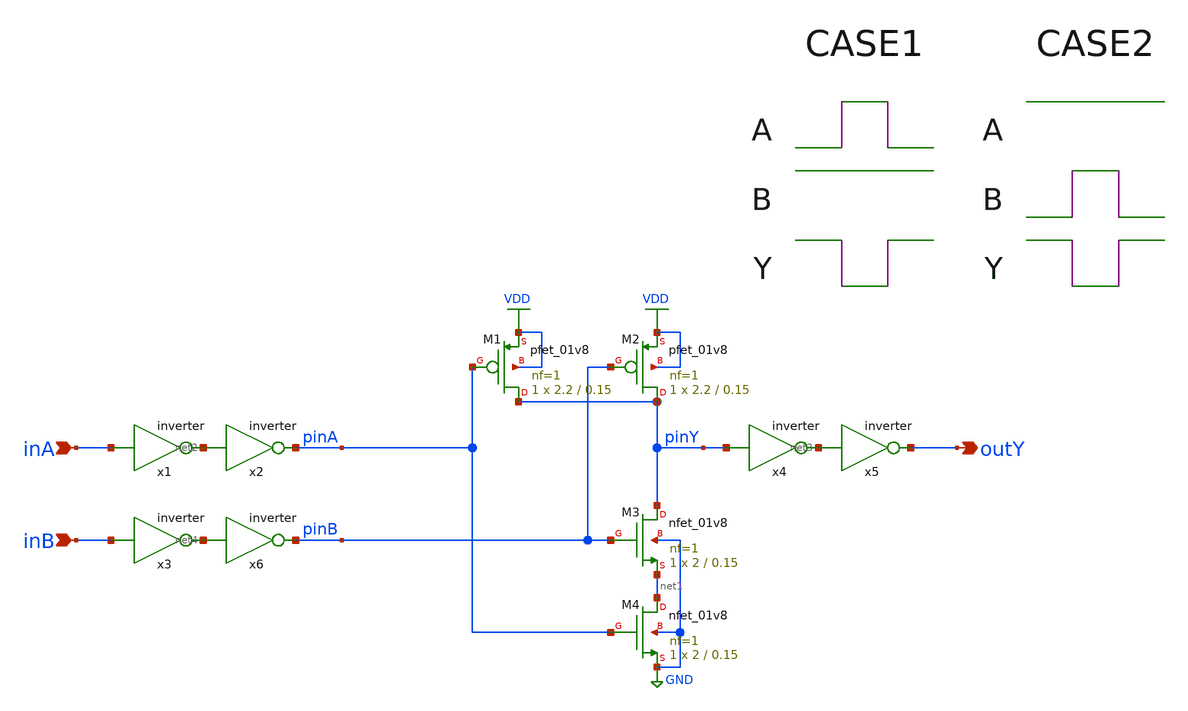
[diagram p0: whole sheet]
** sch_path: nand_delay.sch
**.subckt nand_delay inA outY inB
*.ipin inA
*.opin outY
*.ipin inB
x1 net2 inA inverter
x2 pinA net2 inverter
x4 net3 pinY inverter
x5 outY net3 inverter
x3 net4 inB inverter
x6 pinB net4 inverter
XM1 pinY pinA VDD VDD sky130_fd_pr__pfet_01v8 L=0.15 W=2.2 nf=1 ad='int((nf+1)/2) * W/nf * 0.29' as='int((nf+2)/2) * W/nf * 0.29'
+ pd='2*int((nf+1)/2) * (W/nf + 0.29)' ps='2*int((nf+2)/2) * (W/nf + 0.29)' nrd='0.29 / W' nrs='0.29 / W'
+ sa=0 sb=0 sd=0 mult=1 m=1
XM2 pinY pinB VDD VDD sky130_fd_pr__pfet_01v8 L=0.15 W=2.2 nf=1 ad='int((nf+1)/2) * W/nf * 0.29' as='int((nf+2)/2) * W/nf * 0.29'
+ pd='2*int((nf+1)/2) * (W/nf + 0.29)' ps='2*int((nf+2)/2) * (W/nf + 0.29)' nrd='0.29 / W' nrs='0.29 / W'
+ sa=0 sb=0 sd=0 mult=1 m=1
XM3 pinY pinB net1 GND sky130_fd_pr__nfet_01v8 L=0.15 W=2 nf=1 ad='int((nf+1)/2) * W/nf * 0.29' as='int((nf+2)/2) * W/nf * 0.29'
+ pd='2*int((nf+1)/2) * (W/nf + 0.29)' ps='2*int((nf+2)/2) * (W/nf + 0.29)' nrd='0.29 / W' nrs='0.29 / W'
+ sa=0 sb=0 sd=0 mult=1 m=1
XM4 net1 pinA GND GND sky130_fd_pr__nfet_01v8 L=0.15 W=2 nf=1 ad='int((nf+1)/2) * W/nf * 0.29' as='int((nf+2)/2) * W/nf * 0.29'
+ pd='2*int((nf+1)/2) * (W/nf + 0.29)' ps='2*int((nf+2)/2) * (W/nf + 0.29)' nrd='0.29 / W' nrs='0.29 / W'
+ sa=0 sb=0 sd=0 mult=1 m=1
**** begin user architecture code


VA inA 0 dc 0
VB inB 0 dc 0
VD VDD 0 dc 1.8
.control
alter @va[PULSE] [ 0 1.8 1n 40p 40p 1n 3n ]
alter @vb[PULSE] [ 1.8 1.8 1n 40p 40p 1n 3n ]
tran 10p 3n
meas tran  in1 FIND time WHEN v(pina)=0.9 RISE=1 > NUL
meas tran out1 FIND time WHEN v(piny)=0.9 FALL=1 > NUL
meas tran  in2 FIND time WHEN v(pina)=0.9 FALL=1 > NUL
meas tran out2 FIND time WHEN v(piny)=0.9 RISE=1 > NUL

let calc1 = out1 - in1
set delayna1 = $&calc1
let calc2 = out2 - in2
set delayna2 = $&calc2

alter @vb[PULSE] [ 0 1.8 1n 40p 40p 1n 3n ]
alter @va[PULSE] [ 1.8 1.8 1n 40p 40p 1n 3n ]
tran 10p 3n
meas tran  in5 FIND time WHEN v(pinb)=0.9 RISE=1 > NUL
meas tran out5 FIND time WHEN v(piny)=0.9 FALL=1 > NUL
meas tran  in6 FIND time WHEN v(pinb)=0.9 FALL=1 > NUL
meas tran out6 FIND time WHEN v(piny)=0.9 RISE=1 > NUL

let calc5 = out5 - in5
set delayna5 = $&calc5
let calc6 = out6 - in6
set delayna6 = $&calc6

echo '*** NAND DELAY CASE 1 ***'
echo 'A(LH) when B(H) ='{$delayna1}
echo 'A(HL) when B(H) ='{$delayna2}

echo '*** NAND DELAY CASE 2 ***'
echo 'B(LH) when A(H) ='{$delayna5}
echo 'B(HL) when A(H) ='{$delayna6}

.endc


** opencircuitdesign pdks install
.lib $::SKYWATER_MODELS/sky130.lib.spice tt


**** end user architecture code
**.ends

* expanding   symbol:  inverter.sym # of pins=2
** sym_path: inverter.sym
** sch_path: inverter.sch
.subckt inverter Y A
*.ipin A
*.opin Y
XM1 Y A VDD VDD sky130_fd_pr__pfet_01v8 L=0.15 W=2.2 nf=1 ad='int((nf+1)/2) * W/nf * 0.29' as='int((nf+2)/2) * W/nf * 0.29'
+ pd='2*int((nf+1)/2) * (W/nf + 0.29)' ps='2*int((nf+2)/2) * (W/nf + 0.29)' nrd='0.29 / W' nrs='0.29 / W'
+ sa=0 sb=0 sd=0 mult=1 m=1
XM2 Y A GND GND sky130_fd_pr__nfet_01v8 L=0.15 W=1 nf=1 ad='int((nf+1)/2) * W/nf * 0.29' as='int((nf+2)/2) * W/nf * 0.29'
+ pd='2*int((nf+1)/2) * (W/nf + 0.29)' ps='2*int((nf+2)/2) * (W/nf + 0.29)' nrd='0.29 / W' nrs='0.29 / W'
+ sa=0 sb=0 sd=0 mult=1 m=1
.ends

.GLOBAL VDD
.GLOBAL GND
.end
